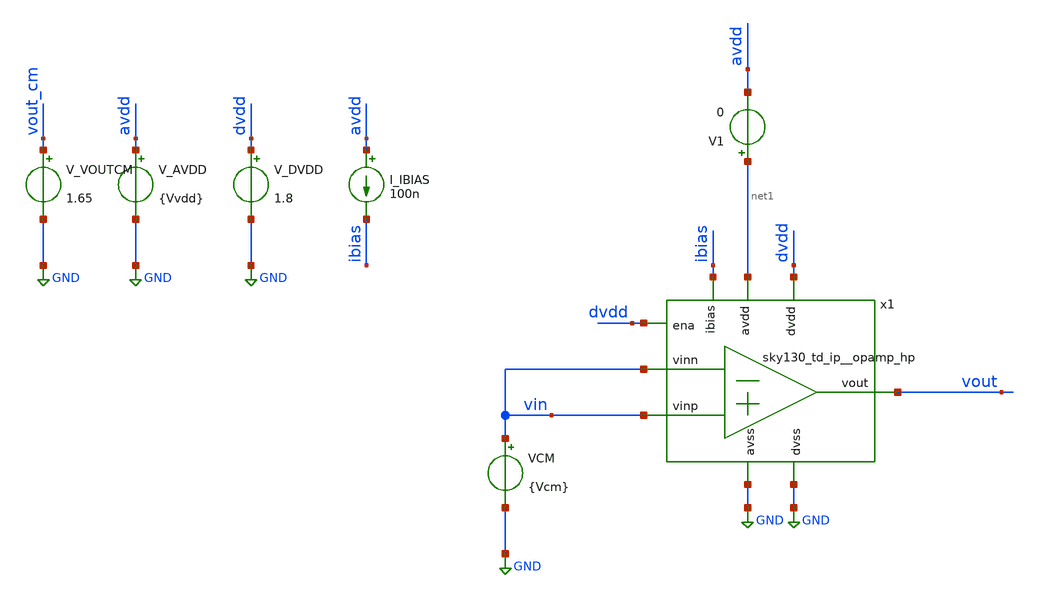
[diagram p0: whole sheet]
** sch_path: cace/ivdd_quiescent.sch
**.subckt ivdd_quiescent
x1 net1 vout ibias vin vin GND dvdd GND dvdd sky130_td_ip__opamp_hp
V_AVDD avdd GND {Vvdd}
.save i(v_avdd)
V_DVDD dvdd GND 1.8
.save i(v_dvdd)
I_IBIAS avdd ibias 100n
V_VOUTCM vout_cm GND 1.65
.save i(v_voutcm)
V1 net1 avdd 0
VCM vin GND {Vcm}
.save i(vcm)
**** begin user architecture code


.control
save all
alter VCM pwl = [ 0 0 10 3.3 ]
alter VCM dc = 0
tran 10m 10
run
let i_avdd = -1 * i(V1)
meas tran max_iavdd MAX i_avdd

echo Max current from AVDD (no load): $&max_iavdd

echo $&max_iavdd > {simpath}/{filename}_{N}.data
quit
.endc




* CACE gensim simulation file {filename}_{N}
* Generated by CACE gensim, Efabless Corporation (c) 2023
* Find the power supply rejection ratio of the amplifier

.include {DUT_path}

.lib {PDK_ROOT}/{PDK}/libs.tech/combined/sky130.lib.spice {corner}

.option TEMP={temperature}
* Flag unsafe operating conditions (exceeds models' specified limits)
.option warn=1
.option SEED=[{seed=12345} + {iterations=0}]


**** end user architecture code
**.ends
.GLOBAL GND
.end
